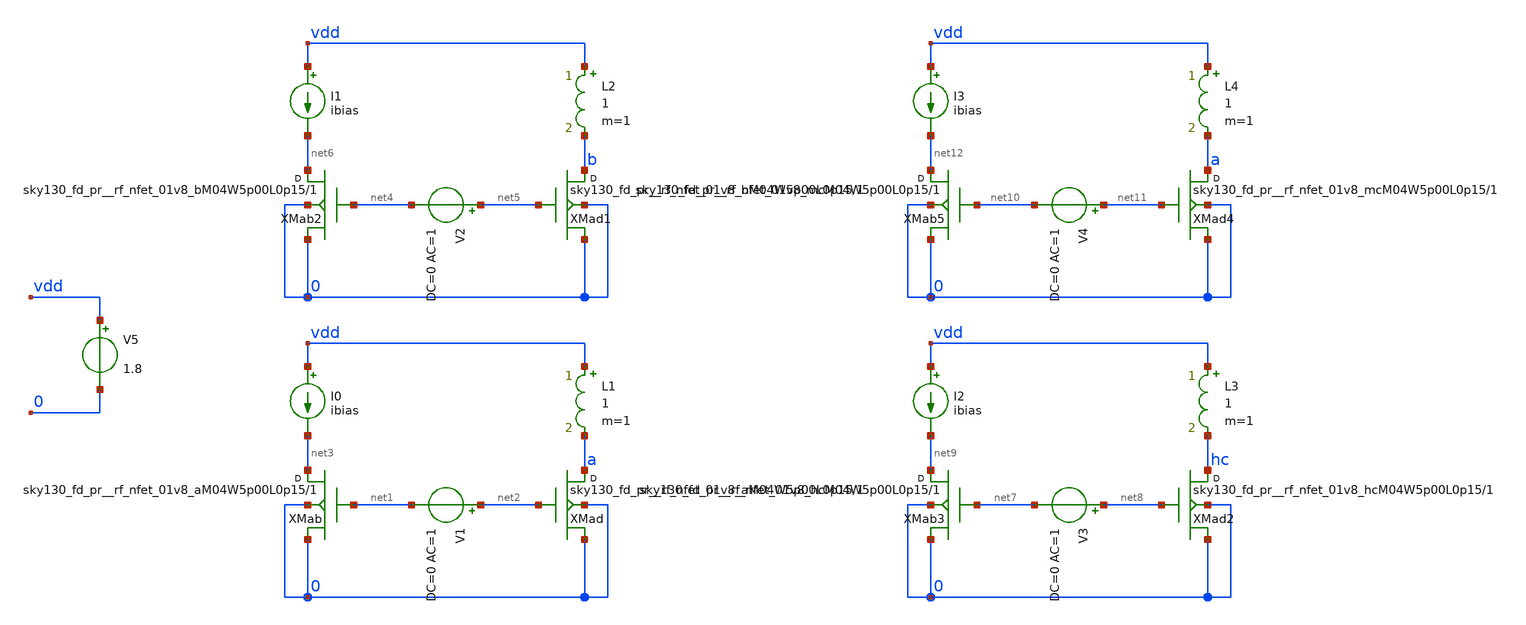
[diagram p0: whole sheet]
** sch_path: design/rfmos_characterise/rfmos_characterise.sch
**.subckt rfmos_characterise
XXMad a net2 0 0 sky130_fd_pr__rf_nfet_01v8_aM04W5p00L0p15 m=1
XXMab net3 net1 0 0 sky130_fd_pr__rf_nfet_01v8_aM04W5p00L0p15 m=1
I0 vdd net3 ibias
V1 net2 net1 DC=0 AC=1
L1 vdd a 1 m=1
XXMad1 b net5 0 0 sky130_fd_pr__rf_nfet_01v8_bM04W5p00L0p15 m=1
XXMab2 net6 net4 0 0 sky130_fd_pr__rf_nfet_01v8_bM04W5p00L0p15 m=1
I1 vdd net6 ibias
V2 net5 net4 DC=0 AC=1
L2 vdd b 1 m=1
XXMad2 hc net8 0 0 sky130_fd_pr__rf_nfet_01v8_hcM04W5p00L0p15 m=1
XXMab3 net9 net7 0 0 sky130_fd_pr__rf_nfet_01v8_hcM04W5p00L0p15 m=1
I2 vdd net9 ibias
V3 net8 net7 DC=0 AC=1
L3 vdd hc 1 m=1
XXMad4 a net11 0 0 sky130_fd_pr__rf_nfet_01v8_mcM04W5p00L0p15 m=1
XXMab5 net12 net10 0 0 sky130_fd_pr__rf_nfet_01v8_mcM04W5p00L0p15 m=1
I3 vdd net12 ibias
V4 net11 net10 DC=0 AC=1
L4 vdd a 1 m=1
V5 vdd 0 1.8
**** begin user architecture code


.param temp=27
.temp 27

.save v(ip) v(in) i(vdd)

.include sky130_fd_pr/cells/rf_nfet_01v8/sky130_fd_pr__rf_nfet_01v8_aM04W5p00L0p15.spice
.include sky130_fd_pr/cells/rf_nfet_01v8/sky130_fd_pr__rf_nfet_01v8_hcM04W5p00L0p15.spice
.include sky130_fd_pr/cells/rf_nfet_01v8/sky130_fd_pr__rf_nfet_01v8_mcM04W5p00L0p15.spice
.include sky130_fd_pr/models/r+c/res_typical__cap_typical__lin.spice
.include sky130_fd_pr/models/r+c/res_typical__cap_typical.spice
*.include sky130_fd_pr/models/corners/tt.spice
.lib sky130_fd_pr/models/sky130.lib.spice tt
*.tran 0.001n 10n uic

.ac dec 10 1 100e9

.param ibais=100e-6


**** end user architecture code
**.ends
.end
